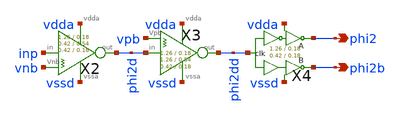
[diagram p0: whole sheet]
** sch_path: xschem/clkgen/phigen_x.sch
**.subckt phigen_x phi2 phi2b
*.opin phi2
*.opin phi2b
X4 phi2dd phi2 phi2b vdda vssd comp_clks Wpmos=1.26 Lpmos=0.18 Wnmos=0.42 Lnmos=0.18
X2 inp phi2d vnb vdda vssd inv_weak_pulldown Wpmos=1.26 Lpmos= Wnmos= Lnmos=0.54
X3 phi2d phi2dd vpb vdda vssd inv_weak_pullup Wpmos=1.26 Lpmos=0.54 Wnmos= Lnmos=
**.ends

* expanding   symbol:  clkgen/comp_clks.sym # of pins=5
** sym_path: xschem/clkgen/comp_clks.sym
** sch_path: xschem/clkgen/comp_clks.sch
.subckt comp_clks clk clka clkb vdd vss  Wpmos=Wpmos Lpmos=Lpmos Wnmos=Wnmos Lnmos=Lnmos
*.ipin clk
*.opin clka
*.opin clkb
*.iopin vdd
*.iopin vss
X1 clk clki vdd vss inv Wpmos=Wpmos Lpmos=Lpmos Wnmos=Wnmos Lnmos=Lnmos
X2 clki clka vdd vss inv Wpmos=Wpmos Lpmos=Lpmos Wnmos=Wnmos Lnmos=Lnmos
X4 clkt clkb vdd vss inv Wpmos=Wpmos Lpmos=Lpmos Wnmos=Wnmos Lnmos=Lnmos
x3 clk clkt vss vdd vdd vss tg Wpmos=Wpmos Lpmos=Lpmos Wnmos=Wnmos Lnmos=Lnmos
.ends


* expanding   symbol:  inv/inv_weak_pulldown.sym # of pins=5
** sym_path: xschem/inv/inv_weak_pulldown.sym
** sch_path: xschem/inv/inv_weak_pulldown.sch
.subckt inv_weak_pulldown in out Vnb vdda vssa  Wpmos=1.26 Lmin=0.18 Wmin=0.42 Lnmos=0.54
*.ipin in
*.iopin out
*.ipin Vnb
*.ipin vdda
*.ipin vssa
XM1 net1 in vssa vssa sky130_fd_pr__nfet_01v8 L=Lmin W=Wmin nf=1 ad='int((nf+1)/2) * W/nf * 0.29' as='int((nf+2)/2) * W/nf * 0.29'
+ pd='2*int((nf+1)/2) * (W/nf + 0.29)' ps='2*int((nf+2)/2) * (W/nf + 0.29)' nrd='0.29 / W' nrs='0.29 / W'
+ sa=0 sb=0 sd=0 mult=1 m=1
XM3 out Vnb net1 vssa sky130_fd_pr__nfet_01v8 L=Lnmos W=Wmin nf=1 ad='int((nf+1)/2) * W/nf * 0.29' as='int((nf+2)/2) * W/nf * 0.29'
+ pd='2*int((nf+1)/2) * (W/nf + 0.29)' ps='2*int((nf+2)/2) * (W/nf + 0.29)' nrd='0.29 / W' nrs='0.29 / W'
+ sa=0 sb=0 sd=0 mult=1 m=1
XM4 out in vdda vdda sky130_fd_pr__pfet_01v8 L=Lmin W=Wpmos nf=1 ad='int((nf+1)/2) * W/nf * 0.29' as='int((nf+2)/2) * W/nf * 0.29'
+ pd='2*int((nf+1)/2) * (W/nf + 0.29)' ps='2*int((nf+2)/2) * (W/nf + 0.29)' nrd='0.29 / W' nrs='0.29 / W'
+ sa=0 sb=0 sd=0 mult=1 m=1
.ends


* expanding   symbol:  inv/inv_weak_pullup.sym # of pins=5
** sym_path: xschem/inv/inv_weak_pullup.sym
** sch_path: xschem/inv/inv_weak_pullup.sch
.subckt inv_weak_pullup in out Vpb vdda vssa  Wpmos=1.26 Lpmos=0.54 Wmin=0.42 Lmin=0.18
*.ipin in
*.iopin out
*.ipin Vpb
*.ipin vdda
*.ipin vssa
XM1 out in vssa vssa sky130_fd_pr__nfet_01v8 L=Lmin W=Wmin nf=1 ad='int((nf+1)/2) * W/nf * 0.29' as='int((nf+2)/2) * W/nf * 0.29'
+ pd='2*int((nf+1)/2) * (W/nf + 0.29)' ps='2*int((nf+2)/2) * (W/nf + 0.29)' nrd='0.29 / W' nrs='0.29 / W'
+ sa=0 sb=0 sd=0 mult=1 m=1
XM3 out Vpb net1 vdda sky130_fd_pr__pfet_01v8 L=Lmin W=Wpmos nf=1 ad='int((nf+1)/2) * W/nf * 0.29' as='int((nf+2)/2) * W/nf * 0.29'
+ pd='2*int((nf+1)/2) * (W/nf + 0.29)' ps='2*int((nf+2)/2) * (W/nf + 0.29)' nrd='0.29 / W' nrs='0.29 / W'
+ sa=0 sb=0 sd=0 mult=1 m=1
XM5 net1 in vdda vdda sky130_fd_pr__pfet_01v8 L=Lmin W=Wpmos nf=1 ad='int((nf+1)/2) * W/nf * 0.29' as='int((nf+2)/2) * W/nf * 0.29'
+ pd='2*int((nf+1)/2) * (W/nf + 0.29)' ps='2*int((nf+2)/2) * (W/nf + 0.29)' nrd='0.29 / W' nrs='0.29 / W'
+ sa=0 sb=0 sd=0 mult=1 m=1
.ends


* expanding   symbol:  xschem/inv/inv.sym # of pins=4
** sym_path: xschem/inv/inv.sym
** sch_path: xschem/inv/inv.sch
.subckt inv in out vdd vss  Wpmos=Wpmos Lpmos=Lpmos Wnmos=Wnmos Lnmos=Lnmos
*.ipin in
*.iopin out
*.iopin vdd
*.iopin vss
XM1 vss in out vss sky130_fd_pr__nfet_01v8 L=Lnmos W=Wnmos nf=1 ad='int((nf+1)/2) * W/nf * 0.29' as='int((nf+2)/2) * W/nf * 0.29'
+ pd='2*int((nf+1)/2) * (W/nf + 0.29)' ps='2*int((nf+2)/2) * (W/nf + 0.29)' nrd='0.29 / W' nrs='0.29 / W'
+ sa=0 sb=0 sd=0 mult=1 m=1
XM2 vdd in out vdd sky130_fd_pr__pfet_01v8 L=Lpmos W=Wpmos nf=1 ad='int((nf+1)/2) * W/nf * 0.29' as='int((nf+2)/2) * W/nf * 0.29'
+ pd='2*int((nf+1)/2) * (W/nf + 0.29)' ps='2*int((nf+2)/2) * (W/nf + 0.29)' nrd='0.29 / W' nrs='0.29 / W'
+ sa=0 sb=0 sd=0 mult=1 m=1
.ends


* expanding   symbol:  xschem/transmission_gate/tg.sym # of pins=6
** sym_path: xschem/transmission_gate/tg.sym
** sch_path: xschem/transmission_gate/tg.sch
.subckt tg in out ctrl_ ctrl vdda vssa  Wpmos=0.42 Lpmos=0.18 Wnmos=0.42 Lnmos=0.18
*.iopin in
*.iopin out
*.ipin ctrl_
*.ipin ctrl
*.ipin vdda
*.ipin vssa
XM1 out ctrl in vssa sky130_fd_pr__nfet_01v8 L=Lnmos W=Wnmos nf=1 ad='int((nf+1)/2) * W/nf * 0.29' as='int((nf+2)/2) * W/nf * 0.29'
+ pd='2*int((nf+1)/2) * (W/nf + 0.29)' ps='2*int((nf+2)/2) * (W/nf + 0.29)' nrd='0.29 / W' nrs='0.29 / W'
+ sa=0 sb=0 sd=0 mult=1 m=1
XM2 out ctrl_ in vdda sky130_fd_pr__pfet_01v8 L=Lpmos W=Wpmos nf=1 ad='int((nf+1)/2) * W/nf * 0.29' as='int((nf+2)/2) * W/nf * 0.29'
+ pd='2*int((nf+1)/2) * (W/nf + 0.29)' ps='2*int((nf+2)/2) * (W/nf + 0.29)' nrd='0.29 / W' nrs='0.29 / W'
+ sa=0 sb=0 sd=0 mult=2 m=2
.ends

.end
